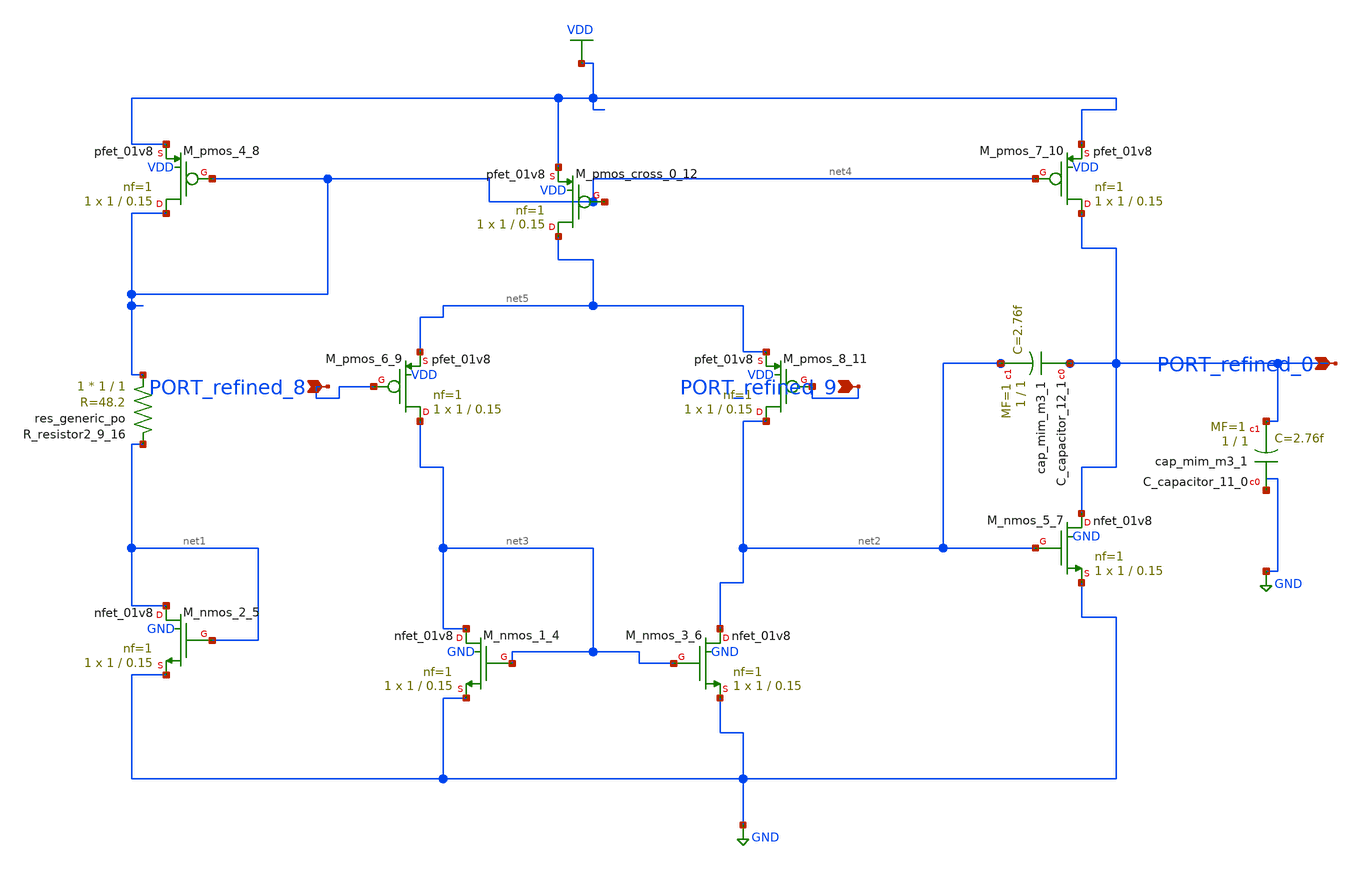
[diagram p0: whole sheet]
** sch_path: schematics/Image2Net/031.sch
**.subckt 031 PORT_refined_8 PORT_refined_0 PORT_refined_9
*.ipin PORT_refined_8
*.ipin PORT_refined_0
*.ipin PORT_refined_9
XC_capacitor_11_0 GND PORT_refined_0 sky130_fd_pr__cap_mim_m3_1 W=1 L=1 MF=1 m=1
XC_capacitor_12_1 PORT_refined_0 net2 sky130_fd_pr__cap_mim_m3_1 W=1 L=1 MF=1 m=1
XM_nmos_1_4 net3 net3 GND GND sky130_fd_pr__nfet_01v8 L=0.15 W=1 nf=1 ad='int((1 + 1)/2) * 1 / 1 * 0.29'
+ as='int((1 + 2)/2) * 1 / 1 * 0.29' pd='2*int((1 + 1)/2) * (1 / 1 + 0.29)' ps='2*int((1 + 2)/2) * (1 / 1 + 0.29)'
+ nrd='0.29 / 1 ' nrs='0.29 / 1 ' sa=0 sb=0 sd=0 mult=1 m=1
XM_nmos_2_5 net1 net1 GND GND sky130_fd_pr__nfet_01v8 L=0.15 W=1 nf=1 ad='int((1 + 1)/2) * 1 / 1 * 0.29'
+ as='int((1 + 2)/2) * 1 / 1 * 0.29' pd='2*int((1 + 1)/2) * (1 / 1 + 0.29)' ps='2*int((1 + 2)/2) * (1 / 1 + 0.29)'
+ nrd='0.29 / 1 ' nrs='0.29 / 1 ' sa=0 sb=0 sd=0 mult=1 m=1
XM_nmos_3_6 net2 net3 GND GND sky130_fd_pr__nfet_01v8 L=0.15 W=1 nf=1 ad='int((1 + 1)/2) * 1 / 1 * 0.29'
+ as='int((1 + 2)/2) * 1 / 1 * 0.29' pd='2*int((1 + 1)/2) * (1 / 1 + 0.29)' ps='2*int((1 + 2)/2) * (1 / 1 + 0.29)'
+ nrd='0.29 / 1 ' nrs='0.29 / 1 ' sa=0 sb=0 sd=0 mult=1 m=1
XM_nmos_5_7 PORT_refined_0 net2 GND GND sky130_fd_pr__nfet_01v8 L=0.15 W=1 nf=1 ad='int((1 + 1)/2) * 1 / 1 * 0.29'
+ as='int((1 + 2)/2) * 1 / 1 * 0.29' pd='2*int((1 + 1)/2) * (1 / 1 + 0.29)' ps='2*int((1 + 2)/2) * (1 / 1 + 0.29)'
+ nrd='0.29 / 1 ' nrs='0.29 / 1 ' sa=0 sb=0 sd=0 mult=1 m=1
XM_pmos_4_8 net4 net4 VDD VDD sky130_fd_pr__pfet_01v8 L=0.15 W=1 nf=1 ad='int((1 + 1)/2) * 1 / 1 * 0.29'
+ as='int((1 + 2)/2) * 1 / 1 * 0.29' pd='2*int((1 + 1)/2) * (1 / 1 + 0.29)' ps='2*int((1 + 2)/2) * (1 / 1 + 0.29)'
+ nrd='0.29 / 1 ' nrs='0.29 / 1 ' sa=0 sb=0 sd=0 mult=1 m=1
XM_pmos_6_9 net3 PORT_refined_8 net5 VDD sky130_fd_pr__pfet_01v8 L=0.15 W=1 nf=1 ad='int((1 + 1)/2) * 1 / 1 * 0.29'
+ as='int((1 + 2)/2) * 1 / 1 * 0.29' pd='2*int((1 + 1)/2) * (1 / 1 + 0.29)' ps='2*int((1 + 2)/2) * (1 / 1 + 0.29)'
+ nrd='0.29 / 1 ' nrs='0.29 / 1 ' sa=0 sb=0 sd=0 mult=1 m=1
XM_pmos_7_10 PORT_refined_0 net4 VDD VDD sky130_fd_pr__pfet_01v8 L=0.15 W=1 nf=1 ad='int((1 + 1)/2) * 1 / 1 * 0.29'
+ as='int((1 + 2)/2) * 1 / 1 * 0.29' pd='2*int((1 + 1)/2) * (1 / 1 + 0.29)' ps='2*int((1 + 2)/2) * (1 / 1 + 0.29)'
+ nrd='0.29 / 1 ' nrs='0.29 / 1 ' sa=0 sb=0 sd=0 mult=1 m=1
XM_pmos_8_11 net2 PORT_refined_9 net5 VDD sky130_fd_pr__pfet_01v8 L=0.15 W=1 nf=1 ad='int((1 + 1)/2) * 1 / 1 * 0.29'
+ as='int((1 + 2)/2) * 1 / 1 * 0.29' pd='2*int((1 + 1)/2) * (1 / 1 + 0.29)' ps='2*int((1 + 2)/2) * (1 / 1 + 0.29)'
+ nrd='0.29 / 1 ' nrs='0.29 / 1 ' sa=0 sb=0 sd=0 mult=1 m=1
XM_pmos_cross_0_12 net5 net4 VDD VDD sky130_fd_pr__pfet_01v8 L=0.15 W=1 nf=1 ad='int((1 + 1)/2) * 1 / 1 * 0.29'
+ as='int((1 + 2)/2) * 1 / 1 * 0.29' pd='2*int((1 + 1)/2) * (1 / 1 + 0.29)' ps='2*int((1 + 2)/2) * (1 / 1 + 0.29)'
+ nrd='0.29 / 1 ' nrs='0.29 / 1 ' sa=0 sb=0 sd=0 mult=1 m=1
XR_resistor2_9_16 net4 net1 sky130_fd_pr__res_generic_po W=1 L=1 m=1
**.ends
.GLOBAL GND
.GLOBAL VDD
.end
